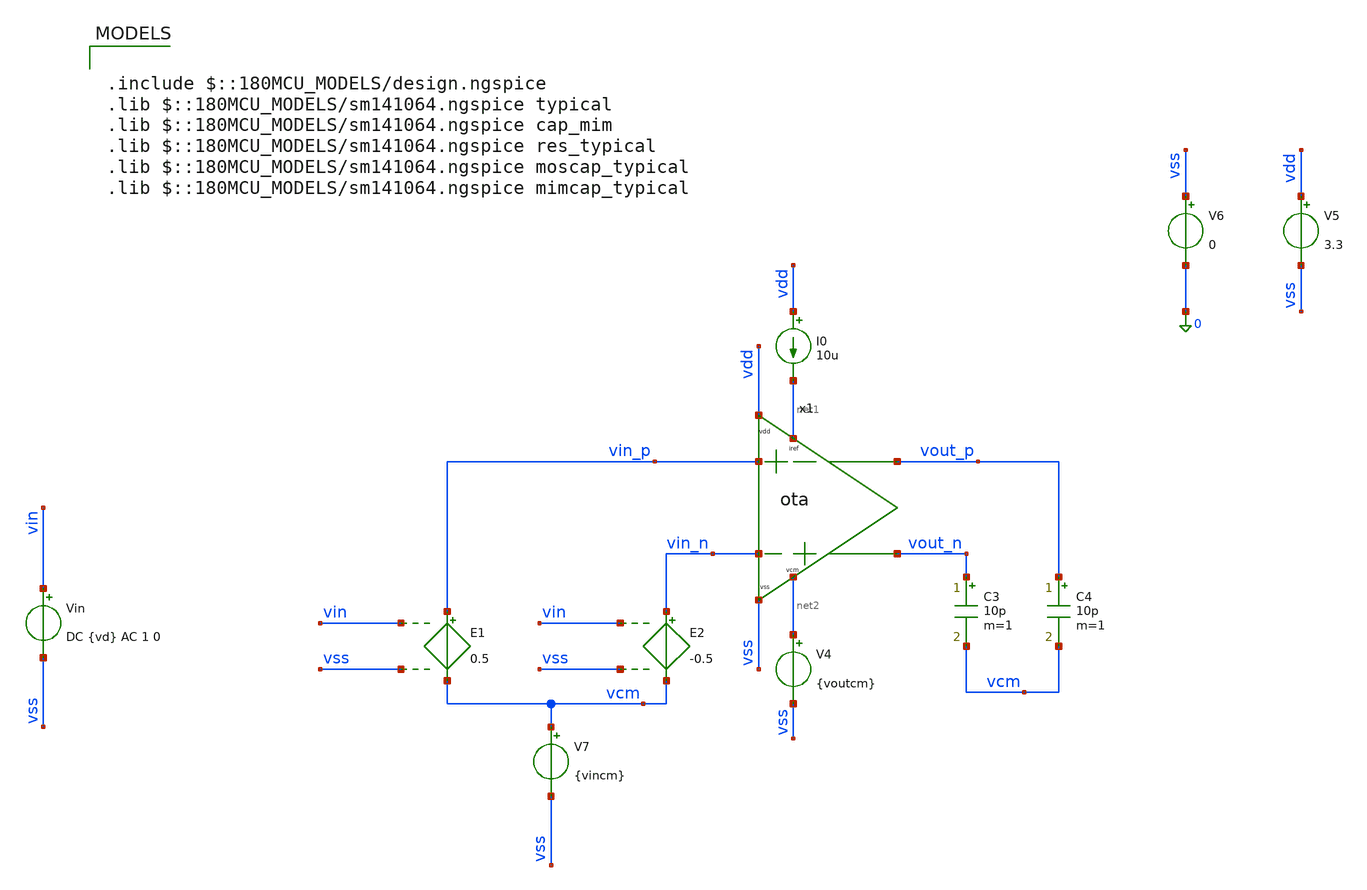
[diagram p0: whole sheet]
** sch_path: xschem/ota/ota_tb.sch
**.subckt ota_tb
x1 vdd net1 vin_p vin_n vss net2 vout_n vout_p ota
I0 vdd net1 10u
V4 net2 vss {voutcm}
C3 vout_n vcm 10p m=1
C4 vout_p vcm 10p m=1
V5 vdd vss 3.3
V6 vss 0 0
V7 vcm vss {vincm}
E1 vin_p vcm vin vss 0.5
E2 vin_n vcm vin vss -0.5
Vin vin vss DC {vd} AC 1 0
**** begin user architecture code

.param vincm=0.5
.param voutcm=1.65
.param vd=0
.control
save all
save @m.x1.x1.xm2.m0[id] @m.x1.x1.xm2.m0[gm] @m.x1.x1.xm2.m0[gds] @m.x1.x1.xm2.m0[cdb]
+ @m.x1.x1.xm2.m0[cgs] @m.x1.x1.xm2.m0[csb] @m.x1.x1.xm2.m0[cgd]
save @m.x1.x1.xm1.m0[id] @m.x1.x1.xm1.m0[gm] @m.x1.x1.xm1.m0[gds] @m.x1.x1.xm1.m0[cdb]
+ @m.x1.x1.xm1.m0[cgs] @m.x1.x1.xm1.m0[csb] @m.x1.x1.xm1.m0[cgd]
save @m.x1.x2.xm1.m0[id] @m.x1.x2.xm1.m0[gm] @m.x1.x2.xm1.m0[gds] @m.x1.x2.xm1.m0[cdb]
+ @m.x1.x2.xm1.m0[cgs] @m.x1.x2.xm1.m0[csb] @m.x1.x2.xm1.m0[cgd]
save @m.x1.x2.xm7.m0[id] @m.x1.x2.xm7.m0[gm] @m.x1.x2.xm7.m0[gds] @m.x1.x2.xm7.m0[cdb]
+ @m.x1.x2.xm7.m0[cgs] @m.x1.x2.xm7.m0[csb] @m.x1.x2.xm7.m0[cgd]
save @m.x1.x2.xm17.m0[id] @m.x1.x2.xm17.m0[gm] @m.x1.x2.xm17.m0[gds] @m.x1.x2.xm17.m0[cdb]
+ @m.x1.x2.xm17.m0[cgs] @m.x1.x2.xm17.m0[csb] @m.x1.x2.xm17.m0[cgd]
save @m.x1.x2.xm18.m0[id] @m.x1.x2.xm18.m0[gm] @m.x1.x2.xm18.m0[gds] @m.x1.x2.xm18.m0[cdb]
+ @m.x1.x2.xm18.m0[cgs] @m.x1.x2.xm18.m0[csb] @m.x1.x2.xm18.m0[cgd]
save @m.x1.x2.xm4.m0[id] @m.x1.x2.xm4.m0[gm] @m.x1.x2.xm4.m0[gds] @m.x1.x2.xm4.m0[cdb]
+ @m.x1.x2.xm4.m0[cgs] @m.x1.x2.xm4.m0[csb] @m.x1.x2.xm4.m0[cgd]
save @m.x1.x2.xm16.m0[id] @m.x1.x2.xm16.m0[gm] @m.x1.x2.xm16.m0[gds] @m.x1.x2.xm16.m0[cdb]
+ @m.x1.x2.xm16.m0[cgs] @m.x1.x2.xm16.m0[csb] @m.x1.x2.xm16.m0[cgd]
save @m.x1.x2.xm19.m0[id] @m.x1.x2.xm19.m0[gm] @m.x1.x2.xm19.m0[gds] @m.x1.x2.xm19.m0[cdb]
+ @m.x1.x2.xm19.m0[cgs] @m.x1.x2.xm19.m0[csb] @m.x1.x2.xm19.m0[cgd]
save @m.x1.x2.xm11.m0[id] @m.x1.x2.xm11.m0[gm] @m.x1.x2.xm11.m0[gds] @m.x1.x2.xm11.m0[cdb]
+ @m.x1.x2.xm11.m0[cgs] @m.x1.x2.xm11.m0[csb] @m.x1.x2.xm11.m0[cgd]
save @m.x1.x2.xm6.m0[id] @m.x1.x2.xm6.m0[gm] @m.x1.x2.xm6.m0[gds] @m.x1.x2.xm6.m0[cdb]
+ @m.x1.x2.xm6.m0[cgs] @m.x1.x2.xm6.m0[csb] @m.x1.x2.xm6.m0[cgd]
save @m.x1.x2.xm25.m0[id] @m.x1.x2.xm25.m0[gm] @m.x1.x2.xm25.m0[gds] @m.x1.x2.xm25.m0[cdb]
+ @m.x1.x2.xm25.m0[cgs] @m.x1.x2.xm25.m0[csb] @m.x1.x2.xm25.m0[cgd]
save @m.x1.x2.xm26.m0[id] @m.x1.x2.xm26.m0[gm] @m.x1.x2.xm26.m0[gds] @m.x1.x2.xm26.m0[cdb]
+ @m.x1.x2.xm26.m0[cgs] @m.x1.x2.xm26.m0[csb] @m.x1.x2.xm26.m0[cgd]
save @m.x1.x2.xm27.m0[id] @m.x1.x2.xm27.m0[gm] @m.x1.x2.xm27.m0[gds] @m.x1.x2.xm27.m0[cdb]
+ @m.x1.x2.xm27.m0[cgs] @m.x1.x2.xm27.m0[csb] @m.x1.x2.xm27.m0[cgd]
save @m.x1.x3.xm14.m0[id] @m.x1.x3.xm14.m0[gm] @m.x1.x3.xm14.m0[gds] @m.x1.x3.xm14.m0[cdb]
+ @m.x1.x3.xm14.m0[cgs] @m.x1.x3.xm14.m0[csb] @m.x1.x3.xm14.m0[cgd]
save @m.x1.x3.xm15.m0[id] @m.x1.x3.xm15.m0[gm] @m.x1.x3.xm15.m0[gds] @m.x1.x3.xm15.m0[cdb]
+ @m.x1.x3.xm15.m0[cgs] @m.x1.x3.xm15.m0[csb] @m.x1.x3.xm15.m0[cgd]
save @m.x1.x3.xm10.m0[id] @m.x1.x3.xm10.m0[gm] @m.x1.x3.xm10.m0[gds] @m.x1.x3.xm10.m0[cdb]
+ @m.x1.x3.xm10.m0[cgs] @m.x1.x3.xm10.m0[csb] @m.x1.x3.xm10.m0[cgd]
save @m.x1.x3.xm5.m0[id] @m.x1.x3.xm5.m0[gm] @m.x1.x3.xm5.m0[gds] @m.x1.x3.xm5.m0[cdb]
+ @m.x1.x3.xm5.m0[cgs] @m.x1.x3.xm5.m0[csb] @m.x1.x3.xm5.m0[cgd]
save @m.x1.x3.xm23.m0[id] @m.x1.x3.xm23.m0[gm] @m.x1.x3.xm23.m0[gds] @m.x1.x3.xm23.m0[cdb]
+ @m.x1.x3.xm23.m0[cgs] @m.x1.x3.xm23.m0[csb] @m.x1.x3.xm23.m0[cgd]
save @m.x1.x3.xm24.m0[id] @m.x1.x3.xm24.m0[gm] @m.x1.x3.xm24.m0[gds] @m.x1.x3.xm24.m0[cdb]
+ @m.x1.x3.xm24.m0[cgs] @m.x1.x3.xm24.m0[csb] @m.x1.x3.xm24.m0[cgd]
save @m.x1.x4.xm9.m0[id] @m.x1.x4.xm9.m0[gm] @m.x1.x4.xm9.m0[gds] @m.x1.x4.xm9.m0[cdb]
+ @m.x1.x4.xm9.m0[cgs] @m.x1.x4.xm9.m0[csb] @m.x1.x4.xm9.m0[cgd]
save @m.x1.x4.xm22.m0[id] @m.x1.x4.xm22.m0[gm] @m.x1.x4.xm22.m0[gds] @m.x1.x4.xm22.m0[cdb]
+ @m.x1.x4.xm22.m0[cgs] @m.x1.x4.xm22.m0[csb] @m.x1.x4.xm22.m0[cgd]
save @m.x1.x4.xm21.m0[id] @m.x1.x4.xm21.m0[gm] @m.x1.x4.xm21.m0[gds] @m.x1.x4.xm21.m0[cdb]
+ @m.x1.x4.xm21.m0[cgs] @m.x1.x4.xm21.m0[csb] @m.x1.x4.xm21.m0[cgd]
save @m.x1.x4.xm8.m0[id] @m.x1.x4.xm8.m0[gm] @m.x1.x4.xm8.m0[gds] @m.x1.x4.xm8.m0[cdb]
+ @m.x1.x4.xm8.m0[cgs] @m.x1.x4.xm8.m0[csb] @m.x1.x4.xm8.m0[cgd]
save @m.x1.x4.xm20.m0[id] @m.x1.x4.xm20.m0[gm] @m.x1.x4.xm20.m0[gds] @m.x1.x4.xm20.m0[cdb]
+ @m.x1.x4.xm20.m0[cgs] @m.x1.x4.xm20.m0[csb] @m.x1.x4.xm20.m0[cgd]
save @m.x1.x5.xm1.m0[id] @m.x1.x5.xm1.m0[gm] @m.x1.x5.xm1.m0[gds] @m.x1.x5.xm1.m0[cdb]
+ @m.x1.x5.xm1.m0[cgs] @m.x1.x5.xm1.m0[csb] @m.x1.x5.xm1.m0[cgd]
save @m.x1.x5.xm2.m0[id] @m.x1.x5.xm2.m0[gm] @m.x1.x5.xm2.m0[gds] @m.x1.x5.xm2.m0[cdb]
+ @m.x1.x5.xm2.m0[cgs] @m.x1.x5.xm2.m0[csb] @m.x1.x5.xm2.m0[cgd]
save @m.x1.x6.xm15.m0[id] @m.x1.x6.xm15.m0[gm] @m.x1.x6.xm15.m0[gds] @m.x1.x6.xm15.m0[cdb]
+ @m.x1.x6.xm15.m0[cgs] @m.x1.x6.xm15.m0[csb] @m.x1.x6.xm15.m0[cgd]
save @m.x1.x6.xm1.m0[id] @m.x1.x6.xm1.m0[gm] @m.x1.x6.xm1.m0[gds] @m.x1.x6.xm1.m0[cdb]
+ @m.x1.x6.xm1.m0[cgs] @m.x1.x6.xm1.m0[csb] @m.x1.x6.xm1.m0[cgd]
save @m.x1.x6.xm2.m0[id] @m.x1.x6.xm2.m0[gm] @m.x1.x6.xm2.m0[gds] @m.x1.x6.xm2.m0[cdb]
+ @m.x1.x6.xm2.m0[cgs] @m.x1.x6.xm2.m0[csb] @m.x1.x6.xm2.m0[cgd]
save @m.x1.x6.xm7.m0[id] @m.x1.x6.xm7.m0[gm] @m.x1.x6.xm7.m0[gds] @m.x1.x6.xm7.m0[cdb]
+ @m.x1.x6.xm7.m0[cgs] @m.x1.x6.xm7.m0[csb] @m.x1.x6.xm7.m0[cgd]
save @m.x1.x6.xm8.m0[id] @m.x1.x6.xm8.m0[gm] @m.x1.x6.xm8.m0[gds] @m.x1.x6.xm8.m0[cdb]
+ @m.x1.x6.xm8.m0[cgs] @m.x1.x6.xm8.m0[csb] @m.x1.x6.xm8.m0[cgd]
save @m.x1.x6.xm4.m0[id] @m.x1.x6.xm4.m0[gm] @m.x1.x6.xm4.m0[gds] @m.x1.x6.xm4.m0[cdb]
+ @m.x1.x6.xm4.m0[cgs] @m.x1.x6.xm4.m0[csb] @m.x1.x6.xm4.m0[cgd]
save @m.x1.x6.xm3.m0[id] @m.x1.x6.xm3.m0[gm] @m.x1.x6.xm3.m0[gds] @m.x1.x6.xm3.m0[cdb]
+ @m.x1.x6.xm3.m0[cgs] @m.x1.x6.xm3.m0[csb] @m.x1.x6.xm3.m0[cgd]
save @m.x1.x6.xm5.m0[id] @m.x1.x6.xm5.m0[gm] @m.x1.x6.xm5.m0[gds] @m.x1.x6.xm5.m0[cdb]
+ @m.x1.x6.xm5.m0[cgs] @m.x1.x6.xm5.m0[csb] @m.x1.x6.xm5.m0[cgd]
save @m.x1.x6.xm6.m0[id] @m.x1.x6.xm6.m0[gm] @m.x1.x6.xm6.m0[gds] @m.x1.x6.xm6.m0[cdb]
+ @m.x1.x6.xm6.m0[cgs] @m.x1.x6.xm6.m0[csb] @m.x1.x6.xm6.m0[cgd]
save @m.x1.x7.xm6.m0[id] @m.x1.x7.xm6.m0[gm] @m.x1.x7.xm6.m0[gds] @m.x1.x7.xm6.m0[cdb]
+ @m.x1.x7.xm6.m0[cgs] @m.x1.x7.xm6.m0[csb] @m.x1.x7.xm6.m0[cgd]
save @m.x1.x7.xm5.m0[id] @m.x1.x7.xm5.m0[gm] @m.x1.x7.xm5.m0[gds] @m.x1.x7.xm5.m0[cdb]
+ @m.x1.x7.xm5.m0[cgs] @m.x1.x7.xm5.m0[csb] @m.x1.x7.xm5.m0[cgd]
save @m.x1.x7.xm1.m0[id] @m.x1.x7.xm1.m0[gm] @m.x1.x7.xm1.m0[gds] @m.x1.x7.xm1.m0[cdb]
+ @m.x1.x7.xm1.m0[cgs] @m.x1.x7.xm1.m0[csb] @m.x1.x7.xm1.m0[cgd]
save @m.x1.x7.xm3.m0[id] @m.x1.x7.xm3.m0[gm] @m.x1.x7.xm3.m0[gds] @m.x1.x7.xm3.m0[cdb]
+ @m.x1.x7.xm3.m0[cgs] @m.x1.x7.xm3.m0[csb] @m.x1.x7.xm3.m0[cgd]
save @m.x1.x7.xm4.m0[id] @m.x1.x7.xm4.m0[gm] @m.x1.x7.xm4.m0[gds] @m.x1.x7.xm4.m0[cdb]
+ @m.x1.x7.xm4.m0[cgs] @m.x1.x7.xm4.m0[csb] @m.x1.x7.xm4.m0[cgd]
save @m.x1.x7.xm2.m0[id] @m.x1.x7.xm2.m0[gm] @m.x1.x7.xm2.m0[gds] @m.x1.x7.xm2.m0[cdb]
+ @m.x1.x7.xm2.m0[cgs] @m.x1.x7.xm2.m0[csb] @m.x1.x7.xm2.m0[cgd]
save @m.x1.x8.xm6.m0[id] @m.x1.x8.xm6.m0[gm] @m.x1.x8.xm6.m0[gds] @m.x1.x8.xm6.m0[cdb]
+ @m.x1.x8.xm6.m0[cgs] @m.x1.x8.xm6.m0[csb] @m.x1.x8.xm6.m0[cgd]
save @m.x1.x8.xm5.m0[id] @m.x1.x8.xm5.m0[gm] @m.x1.x8.xm5.m0[gds] @m.x1.x8.xm5.m0[cdb]
+ @m.x1.x8.xm5.m0[cgs] @m.x1.x8.xm5.m0[csb] @m.x1.x8.xm5.m0[cgd]
save @m.x1.x8.xm1.m0[id] @m.x1.x8.xm1.m0[gm] @m.x1.x8.xm1.m0[gds] @m.x1.x8.xm1.m0[cdb]
+ @m.x1.x8.xm1.m0[cgs] @m.x1.x8.xm1.m0[csb] @m.x1.x8.xm1.m0[cgd]
save @m.x1.x8.xm3.m0[id] @m.x1.x8.xm3.m0[gm] @m.x1.x8.xm3.m0[gds] @m.x1.x8.xm3.m0[cdb]
+ @m.x1.x8.xm3.m0[cgs] @m.x1.x8.xm3.m0[csb] @m.x1.x8.xm3.m0[cgd]
save @m.x1.x8.xm4.m0[id] @m.x1.x8.xm4.m0[gm] @m.x1.x8.xm4.m0[gds] @m.x1.x8.xm4.m0[cdb]
+ @m.x1.x8.xm4.m0[cgs] @m.x1.x8.xm4.m0[csb] @m.x1.x8.xm4.m0[cgd]
save @m.x1.x8.xm2.m0[id] @m.x1.x8.xm2.m0[gm] @m.x1.x8.xm2.m0[gds] @m.x1.x8.xm2.m0[cdb]
+ @m.x1.x8.xm2.m0[cgs] @m.x1.x8.xm2.m0[csb] @m.x1.x8.xm2.m0[cgd]
op
write ota_op.raw all
ac dec 100 1 10G
write ota_ac.raw all
*noise v(vout_p, vout_n) Vin dec 10 1 1000Meg
.endc



.include $::180MCU_MODELS/design.ngspice
.lib $::180MCU_MODELS/sm141064.ngspice typical
.lib $::180MCU_MODELS/sm141064.ngspice cap_mim
.lib $::180MCU_MODELS/sm141064.ngspice res_typical
.lib $::180MCU_MODELS/sm141064.ngspice moscap_typical
.lib $::180MCU_MODELS/sm141064.ngspice mimcap_typical

**** end user architecture code
**.ends
.end
